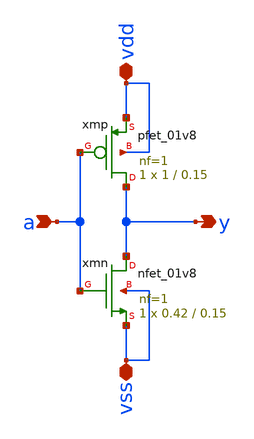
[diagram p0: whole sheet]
** sch_path: research/sky130-layout/toolchain-inverter/inv.sch
**.subckt inv a y vdd vss
*.ipin a
*.opin y
*.iopin vdd
*.iopin vss
Xxmp y a vdd vdd sky130_fd_pr__pfet_01v8 L=0.15 W=1 nf=1 ad='int((nf+1)/2) * W/nf * 0.29' as='int((nf+2)/2) * W/nf * 0.29'
+ pd='2*int((nf+1)/2) * (W/nf + 0.29)' ps='2*int((nf+2)/2) * (W/nf + 0.29)' nrd='0.29 / W' nrs='0.29 / W'
+ sa=0 sb=0 sd=0 mult=1 m=1
Xxmn y a vss vss sky130_fd_pr__nfet_01v8 L=0.15 W=0.42 nf=1 ad='int((1 + 1)/2) * 0.42 / 1 * 0.29' as='int((1 + 2)/2) * 0.42 / 1 * 0.29'
+ pd='2*int((1 + 1)/2) * (0.42 / 1 + 0.29)' ps='2*int((1 + 2)/2) * (0.42 / 1 + 0.29)' nrd='0.29 / 0.42 '
+ nrs='0.29 / 0.42 ' sa=0 sb=0 sd=0 mult=1 m=1
**.ends
.end
